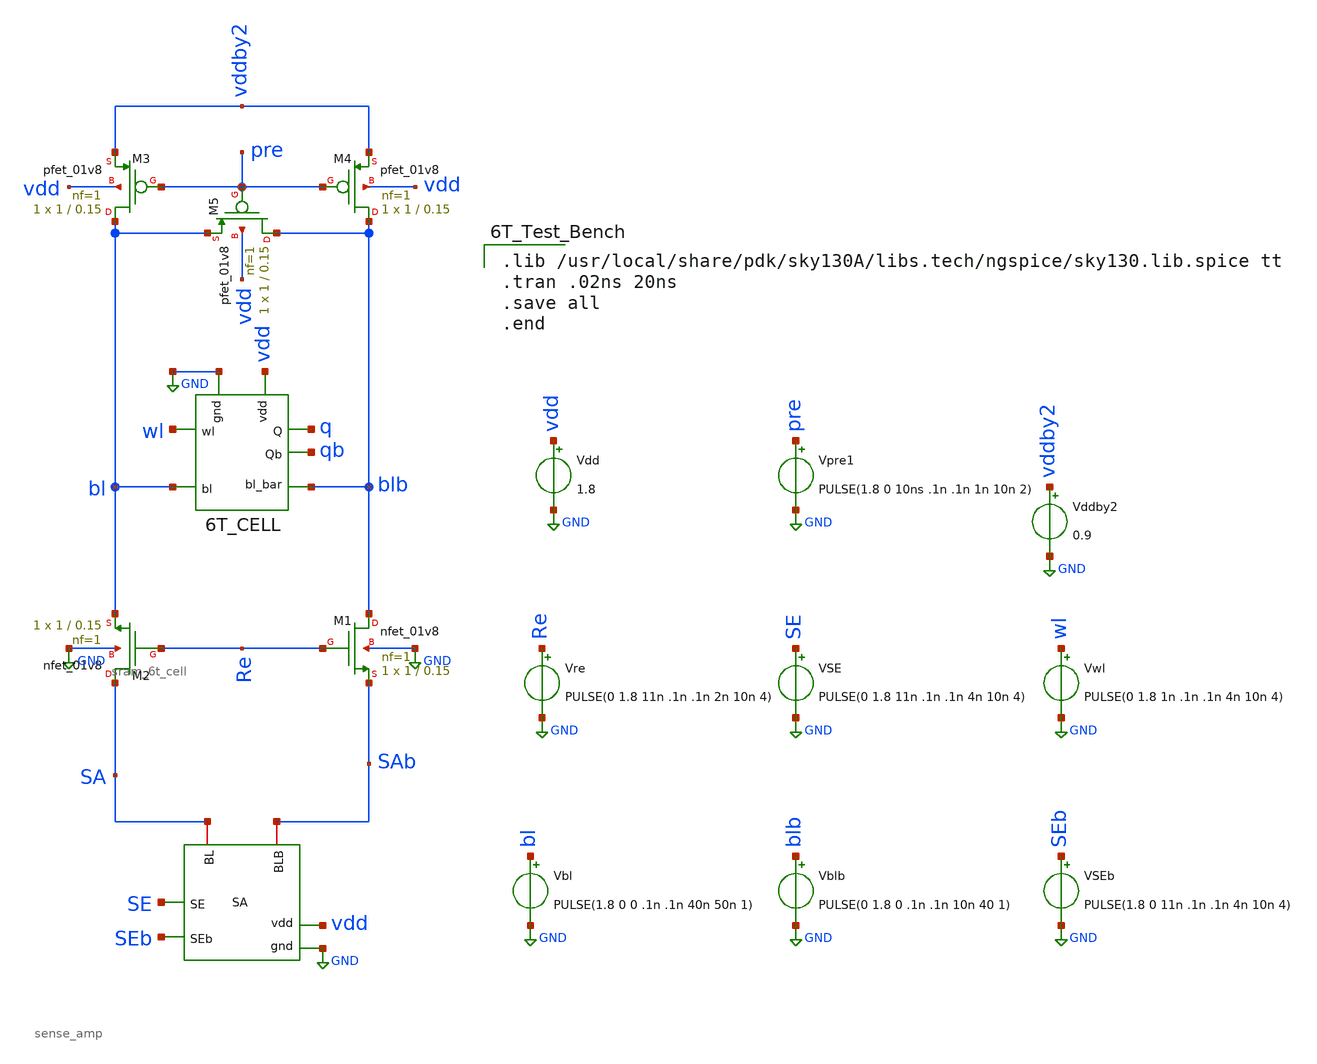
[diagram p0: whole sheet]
** sch_path: Projects/Schematic_Design_and_Analysis_of_an_8-Word_8-Bit_Static_RAM_with_6T_Storage_Cells_using_SKY130PDK/assets/schematic/sense_amp_tb.sch
**.subckt sense_amp_tb
x1 vdd GND SE SEb SA SAb sense_amp
Vdd vdd GND 1.8
Vbl bl GND PULSE(1.8 0 0 .1n .1n 40n 50n 1)
Vblb blb GND PULSE(0 1.8 0 .1n .1n 10n 40 1)
x2 GND vdd wl bl blb q qb sram_6t_cell
Vwl wl GND PULSE(0 1.8 1n .1n .1n 4n 10n 4)
XM1 blb Re SAb GND sky130_fd_pr__nfet_01v8 L=0.15 W=1 nf=1 ad='int((nf+1)/2) * W/nf * 0.29' as='int((nf+2)/2) * W/nf * 0.29'
+ pd='2*int((nf+1)/2) * (W/nf + 0.29)' ps='2*int((nf+2)/2) * (W/nf + 0.29)' nrd='0.29 / W' nrs='0.29 / W'
+ sa=0 sb=0 sd=0 mult=1 m=1
XM2 SA Re bl GND sky130_fd_pr__nfet_01v8 L=0.15 W=1 nf=1 ad='int((nf+1)/2) * W/nf * 0.29' as='int((nf+2)/2) * W/nf * 0.29'
+ pd='2*int((nf+1)/2) * (W/nf + 0.29)' ps='2*int((nf+2)/2) * (W/nf + 0.29)' nrd='0.29 / W' nrs='0.29 / W'
+ sa=0 sb=0 sd=0 mult=1 m=1
XM3 bl pre vddby2 vdd sky130_fd_pr__pfet_01v8 L=0.15 W=1 nf=1 ad='int((nf+1)/2) * W/nf * 0.29' as='int((nf+2)/2) * W/nf * 0.29'
+ pd='2*int((nf+1)/2) * (W/nf + 0.29)' ps='2*int((nf+2)/2) * (W/nf + 0.29)' nrd='0.29 / W' nrs='0.29 / W'
+ sa=0 sb=0 sd=0 mult=1 m=1
XM4 blb pre vddby2 vdd sky130_fd_pr__pfet_01v8 L=0.15 W=1 nf=1 ad='int((nf+1)/2) * W/nf * 0.29' as='int((nf+2)/2) * W/nf * 0.29'
+ pd='2*int((nf+1)/2) * (W/nf + 0.29)' ps='2*int((nf+2)/2) * (W/nf + 0.29)' nrd='0.29 / W' nrs='0.29 / W'
+ sa=0 sb=0 sd=0 mult=1 m=1
XM5 blb pre bl vdd sky130_fd_pr__pfet_01v8 L=0.15 W=1 nf=1 ad='int((nf+1)/2) * W/nf * 0.29' as='int((nf+2)/2) * W/nf * 0.29'
+ pd='2*int((nf+1)/2) * (W/nf + 0.29)' ps='2*int((nf+2)/2) * (W/nf + 0.29)' nrd='0.29 / W' nrs='0.29 / W'
+ sa=0 sb=0 sd=0 mult=1 m=1
Vddby2 vddby2 GND 0.9
Vpre1 pre GND PULSE(1.8 0 10ns .1n .1n 1n 10n 2)
Vre Re GND PULSE(0 1.8 11n .1n .1n 2n 10n 4)
VSE SE GND PULSE(0 1.8 11n .1n .1n 4n 10n 4)
VSEb SEb GND PULSE(1.8 0 11n .1n .1n 4n 10n 4)
**** begin user architecture code

.lib /usr/local/share/pdk/sky130A/libs.tech/ngspice/sky130.lib.spice tt
.tran .02ns 20ns
.save all
.end

**** end user architecture code
**.ends

* expanding   symbol:  sense_amp.sym # of pins=6
** sym_path: Projects/Schematic_Design_and_Analysis_of_an_8-Word_8-Bit_Static_RAM_with_6T_Storage_Cells_using_SKY130PDK/assets/schematic/sense_amp.sym
** sch_path: Projects/Schematic_Design_and_Analysis_of_an_8-Word_8-Bit_Static_RAM_with_6T_Storage_Cells_using_SKY130PDK/assets/schematic/sense_amp.sch
.subckt sense_amp vdd gnd SE SEb BL BLB
*.ipin gnd
*.ipin vdd
*.ipin SE
*.iopin BLB
*.iopin BL
*.ipin SEb
XM1 BL BLB net2 gnd sky130_fd_pr__nfet_01v8 L=0.15 W=2 nf=1 ad='int((nf+1)/2) * W/nf * 0.29' as='int((nf+2)/2) * W/nf * 0.29'
+ pd='2*int((nf+1)/2) * (W/nf + 0.29)' ps='2*int((nf+2)/2) * (W/nf + 0.29)' nrd='0.29 / W' nrs='0.29 / W'
+ sa=0 sb=0 sd=0 mult=1 m=1
XM2 BL BLB net1 vdd sky130_fd_pr__pfet_01v8 L=0.15 W=2 nf=1 ad='int((nf+1)/2) * W/nf * 0.29' as='int((nf+2)/2) * W/nf * 0.29'
+ pd='2*int((nf+1)/2) * (W/nf + 0.29)' ps='2*int((nf+2)/2) * (W/nf + 0.29)' nrd='0.29 / W' nrs='0.29 / W'
+ sa=0 sb=0 sd=0 mult=1 m=1
XM3 BLB BL net2 gnd sky130_fd_pr__nfet_01v8 L=0.15 W=2 nf=1 ad='int((nf+1)/2) * W/nf * 0.29' as='int((nf+2)/2) * W/nf * 0.29'
+ pd='2*int((nf+1)/2) * (W/nf + 0.29)' ps='2*int((nf+2)/2) * (W/nf + 0.29)' nrd='0.29 / W' nrs='0.29 / W'
+ sa=0 sb=0 sd=0 mult=1 m=1
XM4 BLB BL net1 vdd sky130_fd_pr__pfet_01v8 L=0.15 W=2 nf=1 ad='int((nf+1)/2) * W/nf * 0.29' as='int((nf+2)/2) * W/nf * 0.29'
+ pd='2*int((nf+1)/2) * (W/nf + 0.29)' ps='2*int((nf+2)/2) * (W/nf + 0.29)' nrd='0.29 / W' nrs='0.29 / W'
+ sa=0 sb=0 sd=0 mult=1 m=1
XM8 net2 SE gnd gnd sky130_fd_pr__nfet_01v8 L=0.15 W=2 nf=1 ad='int((nf+1)/2) * W/nf * 0.29' as='int((nf+2)/2) * W/nf * 0.29'
+ pd='2*int((nf+1)/2) * (W/nf + 0.29)' ps='2*int((nf+2)/2) * (W/nf + 0.29)' nrd='0.29 / W' nrs='0.29 / W'
+ sa=0 sb=0 sd=0 mult=1 m=1
XM5 vdd SEb net1 vdd sky130_fd_pr__pfet_01v8 L=0.15 W=2 nf=1 ad='int((nf+1)/2) * W/nf * 0.29' as='int((nf+2)/2) * W/nf * 0.29'
+ pd='2*int((nf+1)/2) * (W/nf + 0.29)' ps='2*int((nf+2)/2) * (W/nf + 0.29)' nrd='0.29 / W' nrs='0.29 / W'
+ sa=0 sb=0 sd=0 mult=1 m=1
.ends


* expanding   symbol:  sram_6t_cell.sym # of pins=7
** sym_path: Projects/Schematic_Design_and_Analysis_of_an_8-Word_8-Bit_Static_RAM_with_6T_Storage_Cells_using_SKY130PDK/assets/schematic/sram_6t_cell.sym
** sch_path: Projects/Schematic_Design_and_Analysis_of_an_8-Word_8-Bit_Static_RAM_with_6T_Storage_Cells_using_SKY130PDK/assets/schematic/sram_6t_cell.sch
.subckt sram_6t_cell gnd vdd wl bl bl_bar Q Qb
*.ipin gnd
*.ipin vdd
*.ipin bl_bar
*.ipin bl
*.ipin wl
*.opin Q
*.opin Qb
XM1 Qb Q gnd gnd sky130_fd_pr__nfet_01v8 L=0.15 W=2 nf=1 ad='int((nf+1)/2) * W/nf * 0.29' as='int((nf+2)/2) * W/nf * 0.29'
+ pd='2*int((nf+1)/2) * (W/nf + 0.29)' ps='2*int((nf+2)/2) * (W/nf + 0.29)' nrd='0.29 / W' nrs='0.29 / W'
+ sa=0 sb=0 sd=0 mult=1 m=1
XM2 Qb Q vdd vdd sky130_fd_pr__pfet_01v8 L=0.15 W=1 nf=1 ad='int((nf+1)/2) * W/nf * 0.29' as='int((nf+2)/2) * W/nf * 0.29'
+ pd='2*int((nf+1)/2) * (W/nf + 0.29)' ps='2*int((nf+2)/2) * (W/nf + 0.29)' nrd='0.29 / W' nrs='0.29 / W'
+ sa=0 sb=0 sd=0 mult=1 m=1
XM3 Q Qb gnd gnd sky130_fd_pr__nfet_01v8 L=0.15 W=2 nf=1 ad='int((nf+1)/2) * W/nf * 0.29' as='int((nf+2)/2) * W/nf * 0.29'
+ pd='2*int((nf+1)/2) * (W/nf + 0.29)' ps='2*int((nf+2)/2) * (W/nf + 0.29)' nrd='0.29 / W' nrs='0.29 / W'
+ sa=0 sb=0 sd=0 mult=1 m=1
XM4 Q Qb vdd vdd sky130_fd_pr__pfet_01v8 L=0.15 W=1 nf=1 ad='int((nf+1)/2) * W/nf * 0.29' as='int((nf+2)/2) * W/nf * 0.29'
+ pd='2*int((nf+1)/2) * (W/nf + 0.29)' ps='2*int((nf+2)/2) * (W/nf + 0.29)' nrd='0.29 / W' nrs='0.29 / W'
+ sa=0 sb=0 sd=0 mult=1 m=1
XM5 bl wl Q gnd sky130_fd_pr__nfet_01v8 L=0.15 W=1 nf=1 ad='int((nf+1)/2) * W/nf * 0.29' as='int((nf+2)/2) * W/nf * 0.29'
+ pd='2*int((nf+1)/2) * (W/nf + 0.29)' ps='2*int((nf+2)/2) * (W/nf + 0.29)' nrd='0.29 / W' nrs='0.29 / W'
+ sa=0 sb=0 sd=0 mult=1 m=1
XM6 bl_bar wl Qb gnd sky130_fd_pr__nfet_01v8 L=0.15 W=1 nf=1 ad='int((nf+1)/2) * W/nf * 0.29' as='int((nf+2)/2) * W/nf * 0.29'
+ pd='2*int((nf+1)/2) * (W/nf + 0.29)' ps='2*int((nf+2)/2) * (W/nf + 0.29)' nrd='0.29 / W' nrs='0.29 / W'
+ sa=0 sb=0 sd=0 mult=1 m=1
.ends

.GLOBAL GND
.end
